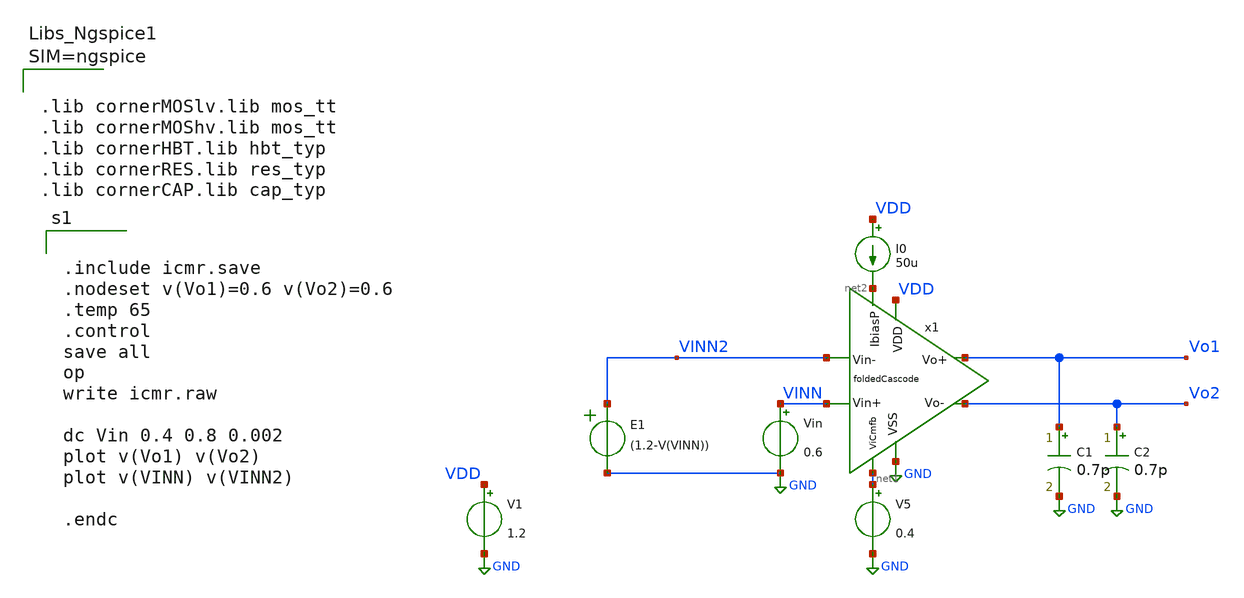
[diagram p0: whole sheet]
** sch_path: sch/tb/icmr.sch
**.subckt icmr
x1 VDD GND net1 net2 Vo1 Vo2 VINN2 VINN foldedCascode
V1 VDD GND 1.2
I0 VDD net2 50u
Vin VINN GND 0.6
C1 Vo1 GND 0.7p m=1
C2 Vo2 GND 0.7p m=1
V5 net1 GND 0.4
E1 VINN2 GND VOL=' (1.2-V(VINN)) '
**** begin user architecture code


.include icmr.save
.nodeset v(Vo1)=0.6 v(Vo2)=0.6
.temp 65
.control
save all
op
write icmr.raw

dc Vin 0.4 0.8 0.002
plot v(Vo1) v(Vo2)
plot v(VINN) v(VINN2)

.endc





.lib cornerMOSlv.lib mos_tt
.lib cornerMOShv.lib mos_tt
.lib cornerHBT.lib hbt_typ
.lib cornerRES.lib res_typ
.lib cornerCAP.lib cap_typ



**** end user architecture code
**.ends

* expanding   symbol:  foldedCascode.sym # of pins=8
** sym_path: sch/blocks/foldedCascode.sym
** sch_path: sch/blocks/foldedCascode.sch
.subckt foldedCascode VDD VSS ViCmfb IbiasP Vo+ Vo- Vin- Vin+
*.iopin VSS
*.iopin VDD
*.ipin ViCmfb
*.iopin IbiasP
*.ipin Vin+
*.ipin Vin-
*.iopin Vo+
*.iopin Vo-
XM11 IbiasP IbiasP VSS VSS sg13_lv_nmos w=2u l=0.3u ng=1 m=1 mm_ok=1
x1 VDD Vb1_1 Vb1_2 Vx Vy VSS gmBoosting
XM0 net3 Vb0 VDD VDD sg13_lv_pmos w=70u l=0.3u ng=120 m=8 mm_ok=1
XM14 Vb3 IbiasP VSS VSS sg13_lv_nmos w=0.5u l=0.3u ng=1 m=1 mm_ok=1
XM15 Vb3 Vb3 VDD VDD sg13_lv_pmos w=4.4u l=0.3u ng=2 m=1 mm_ok=1
XM16 net4 IbiasP VSS VSS sg13_lv_nmos w=0.5u l=0.3u ng=1 m=1 mm_ok=1
XM17 net4 net4 VDD VDD sg13_lv_pmos w=9.5u l=0.3u ng=5 m=1 mm_ok=1
XM1 Vy Vin+ net3 net3 sg13_lv_pmos w=70u l=0.13u ng=100 m=2 mm_ok=1
XM2 Vx Vin- net3 net3 sg13_lv_pmos w=70u l=0.13u ng=100 m=2 mm_ok=1
XM9 net1 Vb3 VDD VDD sg13_lv_pmos w=62u l=0.8u ng=120 m=4 mm_ok=1
XM10 net2 Vb3 VDD VDD sg13_lv_pmos w=62u l=0.8u ng=120 m=4 mm_ok=1
XM7 Vo+ Vb2 net1 VDD sg13_lv_pmos w=63u l=0.4u ng=120 m=4 mm_ok=1
XM3 Vo+ Vb1_1 Vx VSS sg13_lv_nmos w=44u l=0.3u ng=18 m=6 mm_ok=1
V10 Vb0 VSS 0.78
V3 Vb1 GND 0.56
V4 Vb2 GND 0.48
V5 Vb3 GND 0.71
XM8 Vo- Vb2 net2 VDD sg13_lv_pmos w=63u l=0.4u ng=120 m=4 mm_ok=1
XM12 Vx ViCmfb VSS VSS sg13_lv_nmos w=24.2u l=0.8u ng=64 m=6 mm_ok=1
XM4 Vo- Vb1_2 Vy VSS sg13_lv_nmos w=44u l=0.3u ng=18 m=6 mm_ok=1
XM5 Vy ViCmfb VSS VSS sg13_lv_nmos w=24.2u l=0.8u ng=64 m=6 mm_ok=1
.ends


* expanding   symbol:  gmBoosting.sym # of pins=6
** sym_path: sch/blocks/gmBoosting.sym
** sch_path: sch/blocks/gmBoosting.sch
.subckt gmBoosting VDD Vo2 Vo1 Vi+ Vi- VSS
*.iopin VSS
*.opin Vo1
*.opin Vo2
*.ipin Vi+
*.ipin Vi-
*.iopin VDD
V1 Vref VSS 0.55
XM7 net2 Vb4 VDD VDD sg13_lv_pmos w=25u l=0.7u ng=13 m=2 mm_ok=1
XM1 net8 Vi+ net1 net1 sg13_lv_pmos w=40u l=0.15u ng=80 m=4 mm_ok=1
XM2 net4 Vi- net1 net1 sg13_lv_pmos w=40u l=0.15u ng=80 m=4 mm_ok=1
XM0 net1 Vb0 net5 VDD sg13_lv_pmos w=16u l=0.3u ng=20 m=1 mm_ok=1
XM6 net8 Vb3 VSS VSS sg13_lv_nmos w=20u l=0.7u ng=5 m=2 mm_ok=1
XM9 Vo1 Vb2 net2 VDD sg13_lv_pmos w=30u l=0.3u ng=10 m=1 mm_ok=1
XM10 Vo2 Vb2 net3 VDD sg13_lv_pmos w=30u l=0.3u ng=10 m=1 mm_ok=1
XM8 net3 Vb4 VDD VDD sg13_lv_pmos w=25u l=0.7u ng=13 m=2 mm_ok=1
XM3 net5 Vo2 VDD VDD sg13_lv_pmos w=20u l=0.13u ng=5 m=1 mm_ok=1
XM4 net5 Vo1 VDD VDD sg13_lv_pmos w=20u l=0.13u ng=5 m=1 mm_ok=1
XM5 net6 Vref VDD VDD sg13_lv_pmos w=20u l=0.13u ng=5 m=2 mm_ok=1
XM28 Vb0 net7 VSS VSS sg13_lv_nmos w=10u l=0.2u ng=2 m=1 mm_ok=1
XM29 Vb3 Vb3 VSS VSS sg13_lv_nmos w=30u l=0.2u ng=4 m=1 mm_ok=1
XR16 net7 Vb0 sub! rppd w=0.8e-6 l=2.5e-6 m=1 b=0 mm_ok=1
XM30 Vb3 Vb0 net6 VDD sg13_lv_pmos w=16u l=0.3u ng=20 m=1 mm_ok=1
XM31 net4 Vb3 VSS VSS sg13_lv_nmos w=20u l=0.7u ng=5 m=2 mm_ok=1
XM32 Vo1 Vb1 net4 VSS sg13_lv_nmos w=37.5u l=0.7u ng=5 m=1 mm_ok=1
XM33 Vo2 Vb1 net8 VSS sg13_lv_nmos w=37.5u l=0.7u ng=5 m=1 mm_ok=1
XM23 net7 Vbb VDD VDD sg13_lv_pmos w=18u l=1u ng=18 m=1 mm_ok=1
XR9 Vb1 net10 sub! rhigh w=0.5e-6 l=2.31e-6 m=1 b=0 mm_ok=1
XM17 net10 Vb1 net9 VSS sg13_lv_nmos w=25u l=0.7u ng=3 m=1 mm_ok=1
XM18 net9 net10 VSS VSS sg13_lv_nmos w=40u l=0.7u ng=4 m=1 mm_ok=1
XM19 net11 Vb4 VDD VDD sg13_lv_pmos w=15u l=0.7u ng=5 m=1 mm_ok=1
XM20 Vb4 Vb2 net11 VDD sg13_lv_pmos w=7u l=0.3u ng=7 m=1 mm_ok=1
XR10 Vb4 Vb2 sub! rhigh w=0.5e-6 l=1.8e-6 m=1 b=0 mm_ok=1
I3 Vbb VSS 50u
XM21 Vbb Vbb VDD VDD sg13_lv_pmos w=18u l=1u ng=18 m=1 mm_ok=1
XM22 Vb1 Vbb VDD VDD sg13_lv_pmos w=18u l=1u ng=18 m=1 mm_ok=1
XM24 net12 Vbb VDD VDD sg13_lv_pmos w=18u l=1u ng=18 m=1 mm_ok=1
XM25 net12 net12 VSS VSS sg13_lv_nmos w=15u l=1u ng=2 m=1 mm_ok=1
XM26 Vb2 net12 VSS VSS sg13_lv_nmos w=15u l=1u ng=2 m=1 mm_ok=1
.ends

.GLOBAL GND
.end
